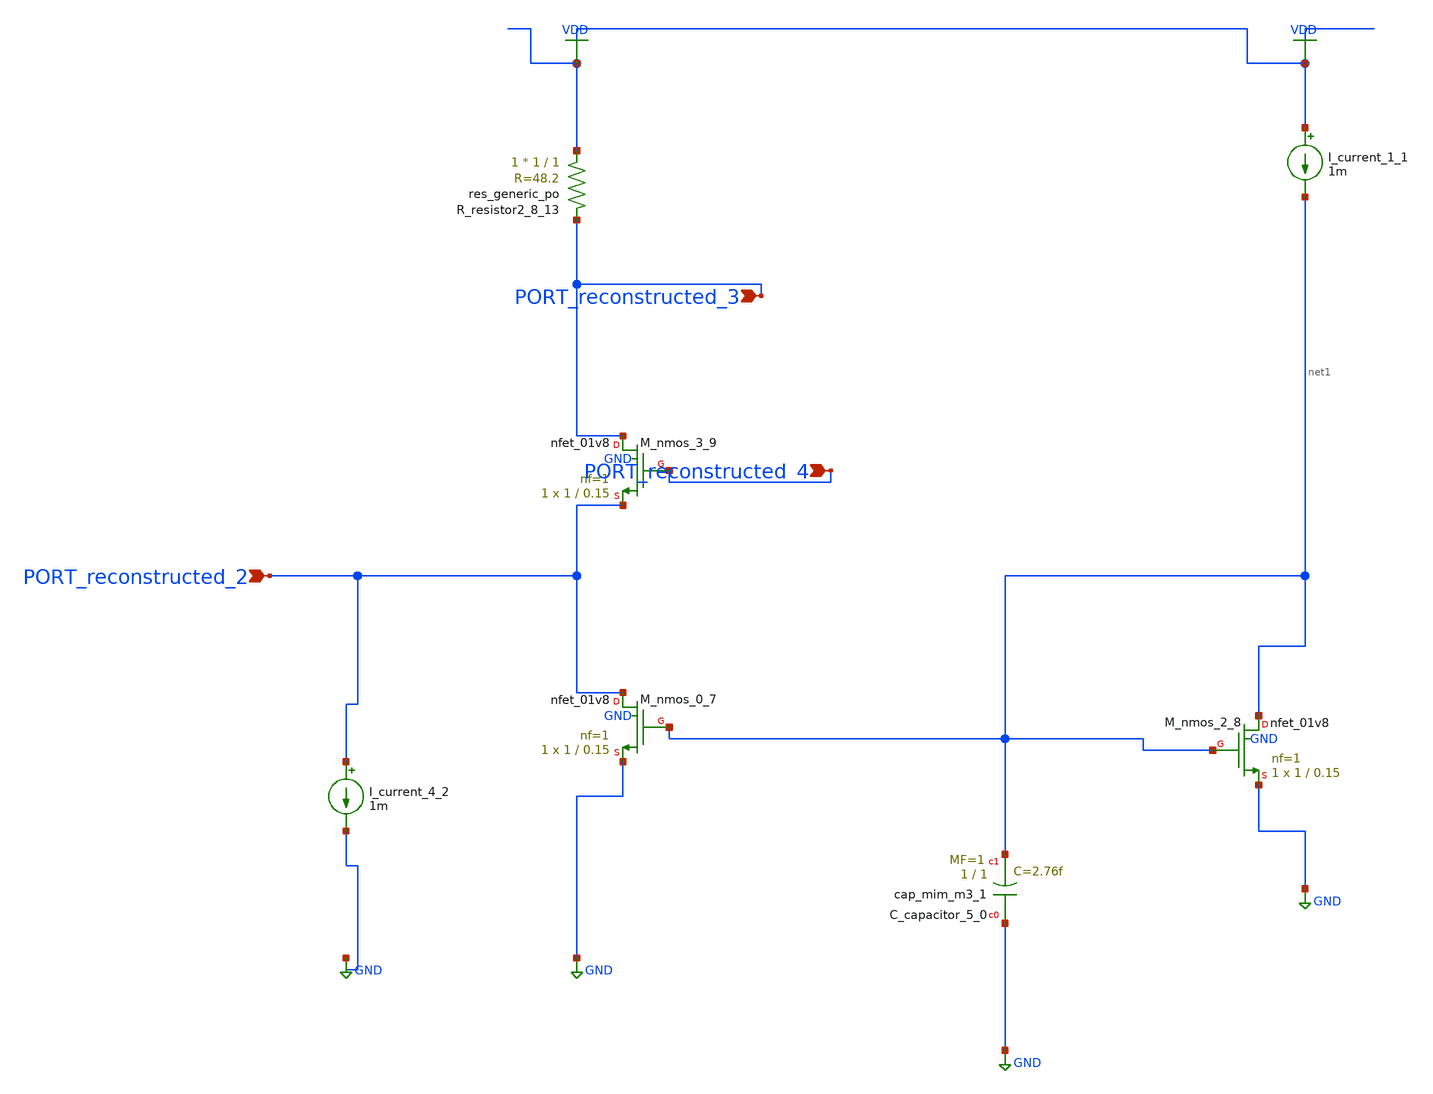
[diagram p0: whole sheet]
** sch_path: schematics/AMSNet/471.sch
**.subckt 471 PORT_reconstructed_4 PORT_reconstructed_3 PORT_reconstructed_2
*.ipin PORT_reconstructed_4
*.ipin PORT_reconstructed_3
*.ipin PORT_reconstructed_2
XC_capacitor_5_0 GND net1 sky130_fd_pr__cap_mim_m3_1 W=1 L=1 MF=1 m=1
I_current_1_1 VDD net1 1m
I_current_4_2 PORT_reconstructed_2 GND 1m
XM_nmos_0_7 PORT_reconstructed_2 net1 GND GND sky130_fd_pr__nfet_01v8 L=0.15 W=1 nf=1 ad='int((1 + 1)/2) * 1 / 1 * 0.29'
+ as='int((1 + 2)/2) * 1 / 1 * 0.29' pd='2*int((1 + 1)/2) * (1 / 1 + 0.29)' ps='2*int((1 + 2)/2) * (1 / 1 + 0.29)'
+ nrd='0.29 / 1 ' nrs='0.29 / 1 ' sa=0 sb=0 sd=0 mult=1 m=1
XM_nmos_2_8 net1 net1 GND GND sky130_fd_pr__nfet_01v8 L=0.15 W=1 nf=1 ad='int((1 + 1)/2) * 1 / 1 * 0.29'
+ as='int((1 + 2)/2) * 1 / 1 * 0.29' pd='2*int((1 + 1)/2) * (1 / 1 + 0.29)' ps='2*int((1 + 2)/2) * (1 / 1 + 0.29)'
+ nrd='0.29 / 1 ' nrs='0.29 / 1 ' sa=0 sb=0 sd=0 mult=1 m=1
XM_nmos_3_9 PORT_reconstructed_3 PORT_reconstructed_4 PORT_reconstructed_2 GND sky130_fd_pr__nfet_01v8
+ L=0.15 W=1 nf=1 ad='int((1 + 1)/2) * 1 / 1 * 0.29' as='int((1 + 2)/2) * 1 / 1 * 0.29' pd='2*int((1 + 1)/2) * (1 / 1 + 0.29)'
+ ps='2*int((1 + 2)/2) * (1 / 1 + 0.29)' nrd='0.29 / 1 ' nrs='0.29 / 1 ' sa=0 sb=0 sd=0 mult=1 m=1
XR_resistor2_8_13 VDD PORT_reconstructed_3 sky130_fd_pr__res_generic_po W=1 L=1 m=1
**.ends
.GLOBAL GND
.GLOBAL VDD
.end
